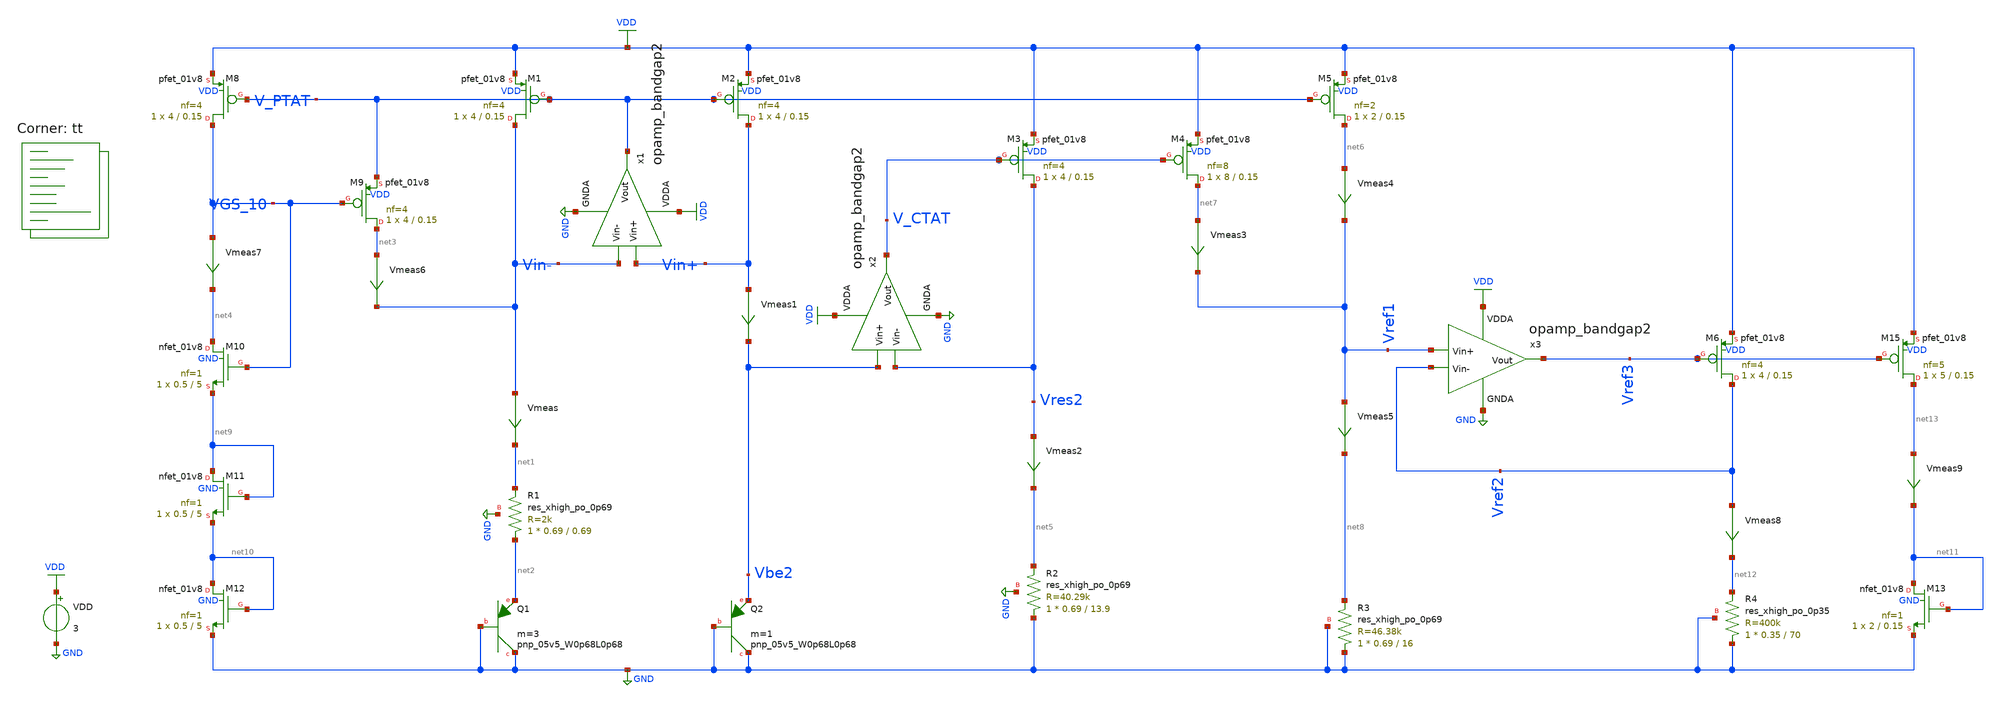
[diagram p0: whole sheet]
** sch_path: projects/pll/bandgapref/xschem_ngspice/mos_bandgap_hajimiri.sch
**.subckt mos_bandgap_hajimiri
VDD VDD GND 3
Vmeas Vin- net1 0
.save i(vmeas)
Vmeas1 Vin+ Vbe2 0
.save i(vmeas1)
x1 VDD V_PTAT Vin- Vin+ GND opamp_bandgap2
XQ1 GND GND net2 sky130_fd_pr__pnp_05v5_W0p68L0p68 m=3
XQ2 GND GND Vbe2 sky130_fd_pr__pnp_05v5_W0p68L0p68 m=1
XR1 net2 net1 GND sky130_fd_pr__res_xhigh_po_0p69 L=0.69 mult=1 m=1
XM1 Vin- V_PTAT VDD VDD sky130_fd_pr__pfet_01v8 L=0.15 W=4 nf=4 ad='int((nf+1)/2) * W/nf * 0.29' as='int((nf+2)/2) * W/nf * 0.29'
+ pd='2*int((nf+1)/2) * (W/nf + 0.29)' ps='2*int((nf+2)/2) * (W/nf + 0.29)' nrd='0.29 / W' nrs='0.29 / W'
+ sa=0 sb=0 sd=0 mult=1 m=1
XM2 Vin+ V_PTAT VDD VDD sky130_fd_pr__pfet_01v8 L=0.15 W=4 nf=4 ad='int((nf+1)/2) * W/nf * 0.29' as='int((nf+2)/2) * W/nf * 0.29'
+ pd='2*int((nf+1)/2) * (W/nf + 0.29)' ps='2*int((nf+2)/2) * (W/nf + 0.29)' nrd='0.29 / W' nrs='0.29 / W'
+ sa=0 sb=0 sd=0 mult=1 m=1
x2 VDD V_CTAT Vres2 Vbe2 GND opamp_bandgap2
XR2 GND net5 GND sky130_fd_pr__res_xhigh_po_0p69 L=13.9 mult=1 m=1
XM3 Vres2 V_CTAT VDD VDD sky130_fd_pr__pfet_01v8 L=0.15 W=4 nf=4 ad='int((nf+1)/2) * W/nf * 0.29' as='int((nf+2)/2) * W/nf * 0.29'
+ pd='2*int((nf+1)/2) * (W/nf + 0.29)' ps='2*int((nf+2)/2) * (W/nf + 0.29)' nrd='0.29 / W' nrs='0.29 / W'
+ sa=0 sb=0 sd=0 mult=1 m=1
XM4 net7 V_CTAT VDD VDD sky130_fd_pr__pfet_01v8 L=0.15 W=8 nf=8 ad='int((nf+1)/2) * W/nf * 0.29' as='int((nf+2)/2) * W/nf * 0.29'
+ pd='2*int((nf+1)/2) * (W/nf + 0.29)' ps='2*int((nf+2)/2) * (W/nf + 0.29)' nrd='0.29 / W' nrs='0.29 / W'
+ sa=0 sb=0 sd=0 mult=1 m=1
XM5 net6 V_PTAT VDD VDD sky130_fd_pr__pfet_01v8 L=0.15 W=2 nf=2 ad='int((nf+1)/2) * W/nf * 0.29' as='int((nf+2)/2) * W/nf * 0.29'
+ pd='2*int((nf+1)/2) * (W/nf + 0.29)' ps='2*int((nf+2)/2) * (W/nf + 0.29)' nrd='0.29 / W' nrs='0.29 / W'
+ sa=0 sb=0 sd=0 mult=1 m=1
XR3 GND net8 GND sky130_fd_pr__res_xhigh_po_0p69 L=16 mult=1 m=1
XM8 VGS_10 V_PTAT VDD VDD sky130_fd_pr__pfet_01v8 L=0.15 W=4 nf=4 ad='int((nf+1)/2) * W/nf * 0.29' as='int((nf+2)/2) * W/nf * 0.29'
+ pd='2*int((nf+1)/2) * (W/nf + 0.29)' ps='2*int((nf+2)/2) * (W/nf + 0.29)' nrd='0.29 / W' nrs='0.29 / W'
+ sa=0 sb=0 sd=0 mult=1 m=1
XM9 net3 VGS_10 V_PTAT VDD sky130_fd_pr__pfet_01v8 L=0.15 W=4 nf=4 ad='int((nf+1)/2) * W/nf * 0.29' as='int((nf+2)/2) * W/nf * 0.29'
+ pd='2*int((nf+1)/2) * (W/nf + 0.29)' ps='2*int((nf+2)/2) * (W/nf + 0.29)' nrd='0.29 / W' nrs='0.29 / W'
+ sa=0 sb=0 sd=0 mult=1 m=1
XM10 net4 VGS_10 net9 GND sky130_fd_pr__nfet_01v8 L=5 W=0.5 nf=1 ad='int((nf+1)/2) * W/nf * 0.29' as='int((nf+2)/2) * W/nf * 0.29'
+ pd='2*int((nf+1)/2) * (W/nf + 0.29)' ps='2*int((nf+2)/2) * (W/nf + 0.29)' nrd='0.29 / W' nrs='0.29 / W'
+ sa=0 sb=0 sd=0 mult=1 m=1
Vmeas2 Vres2 net5 0
.save i(vmeas2)
Vmeas3 net7 Vref1 0
.save i(vmeas3)
Vmeas4 net6 Vref1 0
.save i(vmeas4)
Vmeas5 Vref1 net8 0
.save i(vmeas5)
Vmeas6 net3 Vin- 0
.save i(vmeas6)
Vmeas7 VGS_10 net4 0
.save i(vmeas7)
XM11 net9 net9 net10 GND sky130_fd_pr__nfet_01v8 L=5 W=0.5 nf=1 ad='int((nf+1)/2) * W/nf * 0.29' as='int((nf+2)/2) * W/nf * 0.29'
+ pd='2*int((nf+1)/2) * (W/nf + 0.29)' ps='2*int((nf+2)/2) * (W/nf + 0.29)' nrd='0.29 / W' nrs='0.29 / W'
+ sa=0 sb=0 sd=0 mult=1 m=1
XM12 net10 net10 GND GND sky130_fd_pr__nfet_01v8 L=5 W=0.5 nf=1 ad='int((nf+1)/2) * W/nf * 0.29' as='int((nf+2)/2) * W/nf * 0.29'
+ pd='2*int((nf+1)/2) * (W/nf + 0.29)' ps='2*int((nf+2)/2) * (W/nf + 0.29)' nrd='0.29 / W' nrs='0.29 / W'
+ sa=0 sb=0 sd=0 mult=1 m=1
x3 VDD Vref3 Vref2 Vref1 GND opamp_bandgap2
XM6 Vref2 Vref3 VDD VDD sky130_fd_pr__pfet_01v8 L=0.15 W=4 nf=4 ad='int((nf+1)/2) * W/nf * 0.29' as='int((nf+2)/2) * W/nf * 0.29'
+ pd='2*int((nf+1)/2) * (W/nf + 0.29)' ps='2*int((nf+2)/2) * (W/nf + 0.29)' nrd='0.29 / W' nrs='0.29 / W'
+ sa=0 sb=0 sd=0 mult=1 m=1
XM13 net11 net11 GND GND sky130_fd_pr__nfet_01v8 L=0.15 W=2 nf=1 ad='int((nf+1)/2) * W/nf * 0.29' as='int((nf+2)/2) * W/nf * 0.29'
+ pd='2*int((nf+1)/2) * (W/nf + 0.29)' ps='2*int((nf+2)/2) * (W/nf + 0.29)' nrd='0.29 / W' nrs='0.29 / W'
+ sa=0 sb=0 sd=0 mult=1 m=1
Vmeas8 Vref2 net12 0
.save i(vmeas8)
Vmeas9 net13 net11 0
.save i(vmeas9)
XM15 net13 Vref3 VDD VDD sky130_fd_pr__pfet_01v8 L=0.15 W=5 nf=5 ad='int((nf+1)/2) * W/nf * 0.29' as='int((nf+2)/2) * W/nf * 0.29'
+ pd='2*int((nf+1)/2) * (W/nf + 0.29)' ps='2*int((nf+2)/2) * (W/nf + 0.29)' nrd='0.29 / W' nrs='0.29 / W'
+ sa=0 sb=0 sd=0 mult=1 m=1
XR4 GND net12 GND sky130_fd_pr__res_xhigh_po_0p35 L=70 mult=1 m=1
**** begin user architecture code
.lib $::SKYWATER_MODELS/sky130.lib.spice tt



.option method=gear
.option wnflag=1
.option savecurrents

.save @m.xm1.msky130_fd_pr__pfet_01v8[gm] @m.xm2.msky130_fd_pr__pfet_01v8[gm] @m.xm3.msky130_fd_pr__pfet_01v8[gm] @m.xm4.msky130_fd_pr__pfet_01v8[gm] @m.xm5.msky130_fd_pr__pfet_01v8[gm] @m.xm6.msky130_fd_pr__pfet_01v8[gm] @m.xm7.msky130_fd_pr__pfet_01v8[gm] @m.xm8.msky130_fd_pr__pfet_01v8[gm] @m.xm9.msky130_fd_pr__pfet_01v8[gm] @m.xm10.msky130_fd_pr__nfet_01v8[gm] @m.xm11.msky130_fd_pr__nfet_01v8[gm] @m.xm12.msky130_fd_pr__nfet_01v8[gm]


.control
  save all
  op
  dc temp -40 120 1 VDD 1.6 3.3 0.1
  * tran 1ns 40us
  remzerovec
  write mos_bandgap_hajimiri.raw
  set appendwrite
.endc




**** end user architecture code
**.ends

* expanding   symbol:
*+  /foss/designs/my_design/projects/pll/bandgapref/xschem_ngspice/opamp_bandgap2.sym # of pins=5
** sym_path: projects/bandgapref/xschem_ngspice/old_files/opamp_bandgap2.sym
** sch_path: projects/bandgapref/xschem_ngspice/old_files/opamp_bandgap2.sch
.subckt opamp_bandgap2 VDDA Vout Vin- Vin+ GNDA
*.ipin Vin+
*.opin Vout
*.ipin Vin-
*.ipin GNDA
*.ipin VDDA
XM2 net2 Vin- net1 GNDA sky130_fd_pr__nfet_01v8 L=0.6 W=2 nf=2 ad='int((nf+1)/2) * W/nf * 0.29' as='int((nf+2)/2) * W/nf * 0.29'
+ pd='2*int((nf+1)/2) * (W/nf + 0.29)' ps='2*int((nf+2)/2) * (W/nf + 0.29)' nrd='0.29 / W' nrs='0.29 / W'
+ sa=0 sb=0 sd=0 mult=1 m=1
XM3 Vout Vin+ net1 GNDA sky130_fd_pr__nfet_01v8 L=0.6 W=2 nf=2 ad='int((nf+1)/2) * W/nf * 0.29' as='int((nf+2)/2) * W/nf * 0.29'
+ pd='2*int((nf+1)/2) * (W/nf + 0.29)' ps='2*int((nf+2)/2) * (W/nf + 0.29)' nrd='0.29 / W' nrs='0.29 / W'
+ sa=0 sb=0 sd=0 mult=1 m=1
XM1 net1 net1 GNDA GNDA sky130_fd_pr__nfet_01v8 L=0.6 W=4 nf=1 ad='int((nf+1)/2) * W/nf * 0.29' as='int((nf+2)/2) * W/nf * 0.29'
+ pd='2*int((nf+1)/2) * (W/nf + 0.29)' ps='2*int((nf+2)/2) * (W/nf + 0.29)' nrd='0.29 / W' nrs='0.29 / W'
+ sa=0 sb=0 sd=0 mult=1 m=1
XM4 Vout net2 VDDA VDDA sky130_fd_pr__pfet_01v8 L=0.6 W=4 nf=4 ad='int((nf+1)/2) * W/nf * 0.29' as='int((nf+2)/2) * W/nf * 0.29'
+ pd='2*int((nf+1)/2) * (W/nf + 0.29)' ps='2*int((nf+2)/2) * (W/nf + 0.29)' nrd='0.29 / W' nrs='0.29 / W'
+ sa=0 sb=0 sd=0 mult=1 m=1
XM5 net2 net2 VDDA VDDA sky130_fd_pr__pfet_01v8 L=0.6 W=4 nf=4 ad='int((nf+1)/2) * W/nf * 0.29' as='int((nf+2)/2) * W/nf * 0.29'
+ pd='2*int((nf+1)/2) * (W/nf + 0.29)' ps='2*int((nf+2)/2) * (W/nf + 0.29)' nrd='0.29 / W' nrs='0.29 / W'
+ sa=0 sb=0 sd=0 mult=1 m=1
.ends

.GLOBAL GND
.GLOBAL VDD
.end
